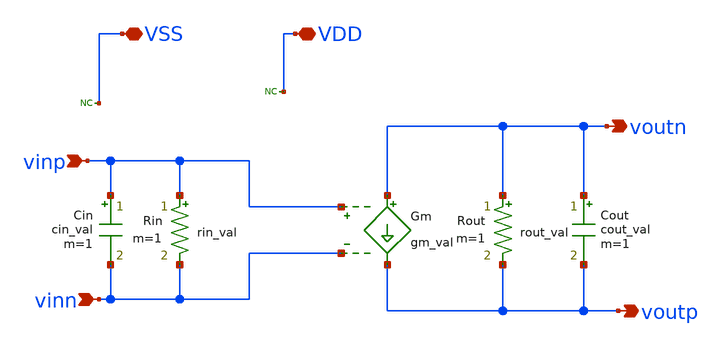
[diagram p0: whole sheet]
** sch_path: analog-db/circuits/amp_028_ideal_fully_diff/pdk/ihp-sg13g2/schematic/ideal-amp-fully-diff.sch
* Copyright 2026 MacAnalog Research Group
**.subckt ideal-amp-fully-diff vinp vinn voutp voutn VDD VSS
*.ipin vinp
*.ipin vinn
*.opin voutp
*.opin voutn
*.iopin VDD
*.iopin VSS
Gm voutn voutp vinp vinn gm_val
Rout voutn voutp rout_val m=1
Rin vinp vinn rin_val m=1
Cout voutn voutp cout_val m=1
Cin vinp vinn cin_val m=1
* noconn VDD
* noconn VSS
**.ends
.end
